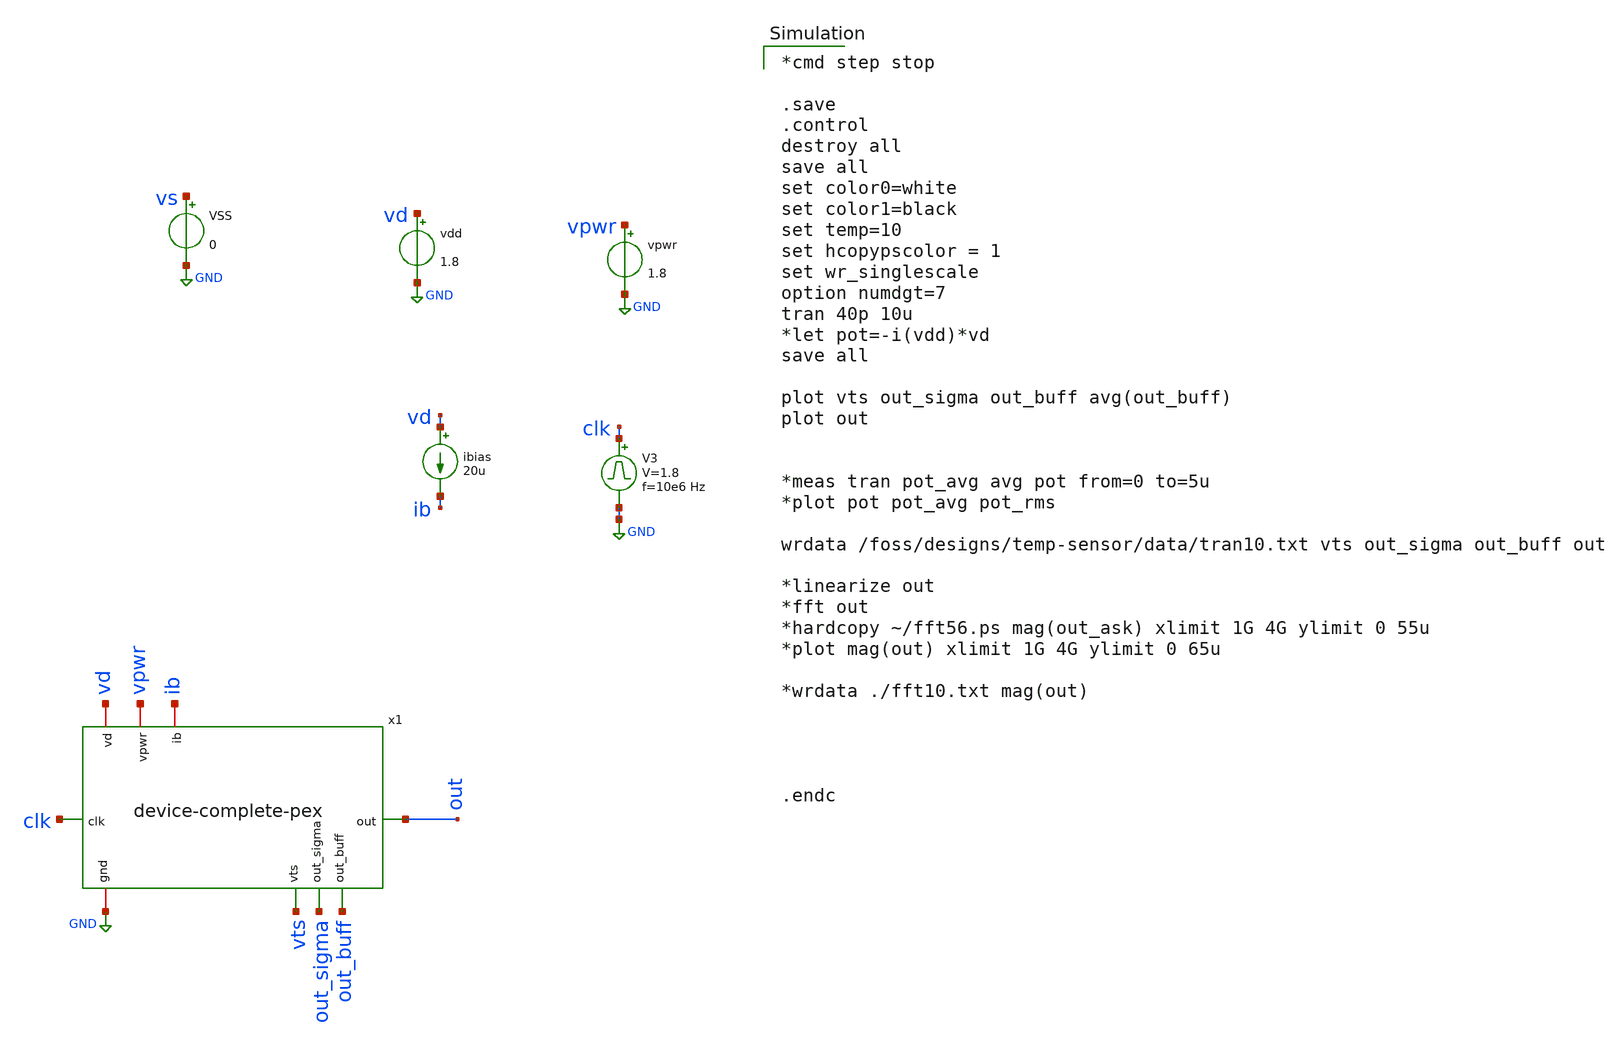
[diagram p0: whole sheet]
** sch_path: device-complete/xschem/device-complete-tb3.sch
**.subckt device-complete-tb3
vpwr vpwr GND 1.8
V3 clk GND pulse 0 1.8 '0.495/ 10e6 ' '0.01/10e6 ' '0.01/10e6 ' '0.49/10e6 ' '1/10e6 '
vdd vd GND 1.8
ibias vd ib 20u
VSS vs GND 0
x1 vd clk out vpwr ib GND out_buff out_sigma vts device-complete-pex
**** begin user architecture code

*cmd step stop

.save
.control
destroy all
save all
set color0=white
set color1=black
set temp=10
set hcopypscolor = 1
set wr_singlescale
option numdgt=7
tran 40p 10u
*let pot=-i(vdd)*vd
save all

plot vts out_sigma out_buff avg(out_buff)
plot out


*meas tran pot_avg avg pot from=0 to=5u
*plot pot pot_avg pot_rms

wrdata /foss/designs/temp-sensor/data/tran10.txt vts out_sigma out_buff out

*linearize out
*fft out
*hardcopy ~/fft56.ps mag(out_ask) xlimit 1G 4G ylimit 0 55u
*plot mag(out) xlimit 1G 4G ylimit 0 65u

*wrdata ./fft10.txt mag(out)




.endc



 .lib $::SKYWATER_MODELS/sky130.lib.spice tt
.include $::SKYWATER_STDCELLS/sky130_fd_sc_hd.spice

**** end user architecture code
**.ends
.GLOBAL GND
.end
